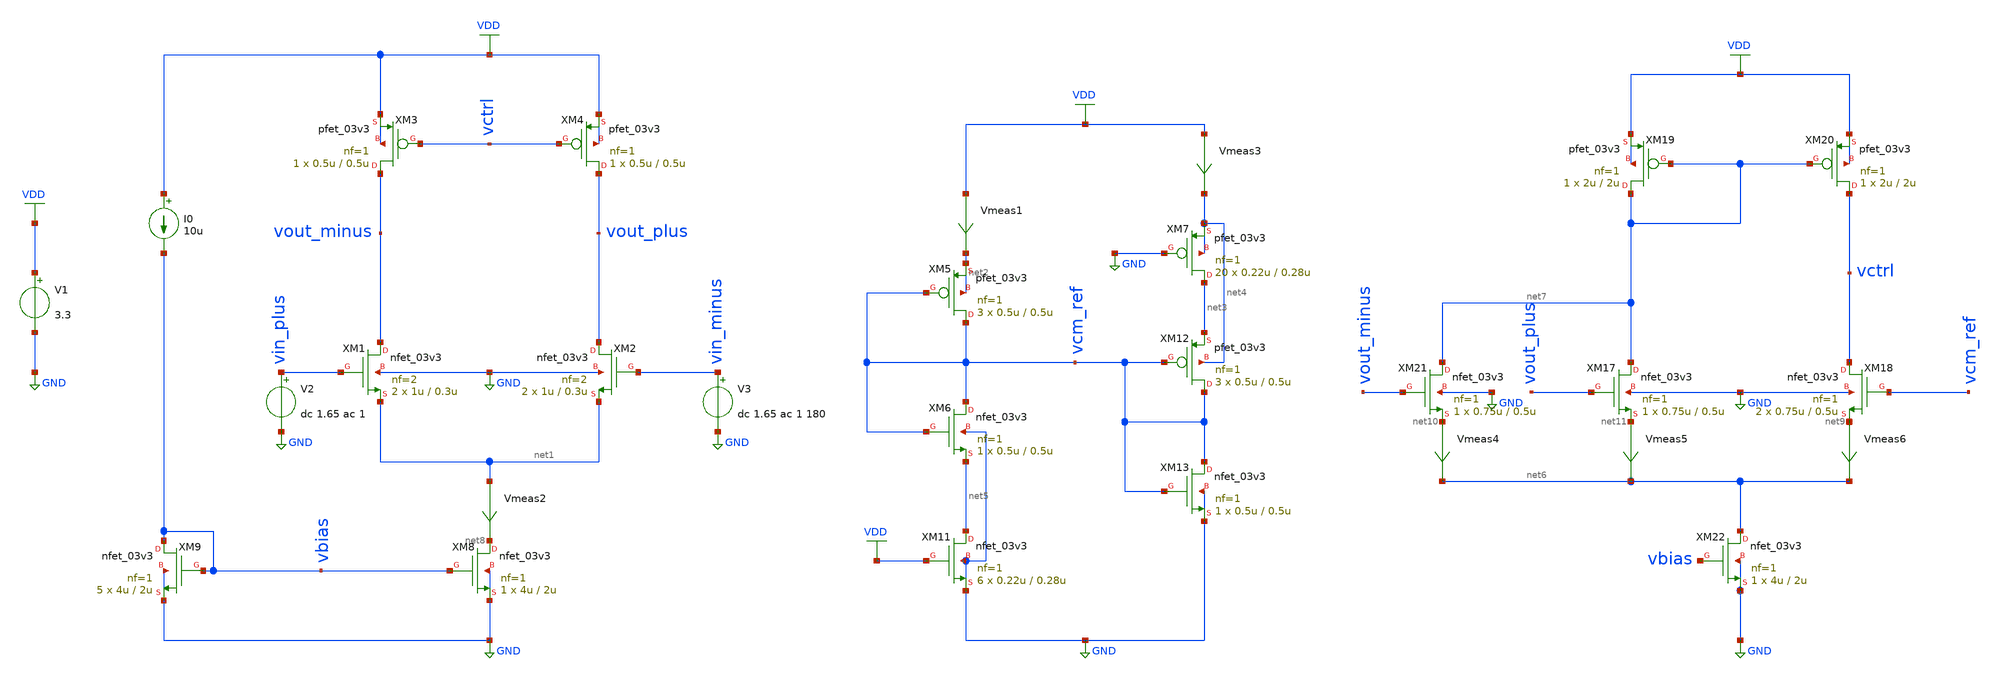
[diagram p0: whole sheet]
** sch_path: Design_Files/RAMP_test_try1.sch
**.subckt RAMP_test_try1
XM1 vout_minus vin_plus net1 GND nfet_03v3 L=0.3u W=1u nf=2 ad='int((nf+1)/2) * W/nf * 0.18u' as='int((nf+2)/2) * W/nf * 0.18u'
+ pd='2*int((nf+1)/2) * (W/nf + 0.18u)' ps='2*int((nf+2)/2) * (W/nf + 0.18u)' nrd='0.18u / W' nrs='0.18u / W'
+ sa=0 sb=0 sd=0 m=2
XM3 vout_minus vctrl VDD VDD pfet_03v3 L=0.5u W=0.5u nf=1 ad='int((nf+1)/2) * W/nf * 0.18u' as='int((nf+2)/2) * W/nf * 0.18u'
+ pd='2*int((nf+1)/2) * (W/nf + 0.18u)' ps='2*int((nf+2)/2) * (W/nf + 0.18u)' nrd='0.18u / W' nrs='0.18u / W'
+ sa=0 sb=0 sd=0 m=1
V2 vin_plus GND dc 1.65 ac 1
XM8 net8 vbias GND GND nfet_03v3 L=2u W=4u nf=1 ad='int((nf+1)/2) * W/nf * 0.18u' as='int((nf+2)/2) * W/nf * 0.18u'
+ pd='2*int((nf+1)/2) * (W/nf + 0.18u)' ps='2*int((nf+2)/2) * (W/nf + 0.18u)' nrd='0.18u / W' nrs='0.18u / W'
+ sa=0 sb=0 sd=0 m=1
Vmeas2 net1 net8 0
.save i(vmeas2)
V3 vin_minus GND dc 1.65 ac 1 180
XM9 vbias vbias GND GND nfet_03v3 L=2u W=4u nf=1 ad='int((nf+1)/2) * W/nf * 0.18u' as='int((nf+2)/2) * W/nf * 0.18u'
+ pd='2*int((nf+1)/2) * (W/nf + 0.18u)' ps='2*int((nf+2)/2) * (W/nf + 0.18u)' nrd='0.18u / W' nrs='0.18u / W'
+ sa=0 sb=0 sd=0 m=5
I0 VDD vbias 10u
XM2 vout_plus vin_minus net1 GND nfet_03v3 L=0.3u W=1u nf=2 ad='int((nf+1)/2) * W/nf * 0.18u' as='int((nf+2)/2) * W/nf * 0.18u'
+ pd='2*int((nf+1)/2) * (W/nf + 0.18u)' ps='2*int((nf+2)/2) * (W/nf + 0.18u)' nrd='0.18u / W' nrs='0.18u / W'
+ sa=0 sb=0 sd=0 m=2
XM4 vout_plus vctrl VDD VDD pfet_03v3 L=0.5u W=0.5u nf=1 ad='int((nf+1)/2) * W/nf * 0.18u' as='int((nf+2)/2) * W/nf * 0.18u'
+ pd='2*int((nf+1)/2) * (W/nf + 0.18u)' ps='2*int((nf+2)/2) * (W/nf + 0.18u)' nrd='0.18u / W' nrs='0.18u / W'
+ sa=0 sb=0 sd=0 m=1
V1 VDD GND 3.3
Vmeas1 VDD net2 0
.save i(vmeas1)
Vmeas3 VDD net4 0
.save i(vmeas3)
XM5 vcm_ref vcm_ref net2 net2 pfet_03v3 L=0.5u W=0.5u nf=1 ad='int((nf+1)/2) * W/nf * 0.18u' as='int((nf+2)/2) * W/nf * 0.18u'
+ pd='2*int((nf+1)/2) * (W/nf + 0.18u)' ps='2*int((nf+2)/2) * (W/nf + 0.18u)' nrd='0.18u / W' nrs='0.18u / W'
+ sa=0 sb=0 sd=0 m=3
XM6 vcm_ref vcm_ref net5 GND nfet_03v3 L=0.5u W=0.5u nf=1 ad='int((nf+1)/2) * W/nf * 0.18u' as='int((nf+2)/2) * W/nf * 0.18u'
+ pd='2*int((nf+1)/2) * (W/nf + 0.18u)' ps='2*int((nf+2)/2) * (W/nf + 0.18u)' nrd='0.18u / W' nrs='0.18u / W'
+ sa=0 sb=0 sd=0 m=1
XM11 net5 VDD GND GND nfet_03v3 L=0.28u W=0.22u nf=1 ad='int((nf+1)/2) * W/nf * 0.18u' as='int((nf+2)/2) * W/nf * 0.18u'
+ pd='2*int((nf+1)/2) * (W/nf + 0.18u)' ps='2*int((nf+2)/2) * (W/nf + 0.18u)' nrd='0.18u / W' nrs='0.18u / W'
+ sa=0 sb=0 sd=0 m=6
XM13 vcm_ref vcm_ref GND GND nfet_03v3 L=0.5u W=0.5u nf=1 ad='int((nf+1)/2) * W/nf * 0.18u' as='int((nf+2)/2) * W/nf * 0.18u'
+ pd='2*int((nf+1)/2) * (W/nf + 0.18u)' ps='2*int((nf+2)/2) * (W/nf + 0.18u)' nrd='0.18u / W' nrs='0.18u / W'
+ sa=0 sb=0 sd=0 m=1
XM12 vcm_ref vcm_ref net3 net4 pfet_03v3 L=0.5u W=0.5u nf=1 ad='int((nf+1)/2) * W/nf * 0.18u' as='int((nf+2)/2) * W/nf * 0.18u'
+ pd='2*int((nf+1)/2) * (W/nf + 0.18u)' ps='2*int((nf+2)/2) * (W/nf + 0.18u)' nrd='0.18u / W' nrs='0.18u / W'
+ sa=0 sb=0 sd=0 m=3
XM7 net3 GND net4 net4 pfet_03v3 L=0.28u W=0.22u nf=1 ad='int((nf+1)/2) * W/nf * 0.18u' as='int((nf+2)/2) * W/nf * 0.18u'
+ pd='2*int((nf+1)/2) * (W/nf + 0.18u)' ps='2*int((nf+2)/2) * (W/nf + 0.18u)' nrd='0.18u / W' nrs='0.18u / W'
+ sa=0 sb=0 sd=0 m=20
XM18 vctrl vcm_ref net9 GND nfet_03v3 L=0.5u W=0.75u nf=1 ad='int((nf+1)/2) * W/nf * 0.18u' as='int((nf+2)/2) * W/nf * 0.18u'
+ pd='2*int((nf+1)/2) * (W/nf + 0.18u)' ps='2*int((nf+2)/2) * (W/nf + 0.18u)' nrd='0.18u / W' nrs='0.18u / W'
+ sa=0 sb=0 sd=0 m=2
XM19 net7 net7 VDD VDD pfet_03v3 L=2u W=2u nf=1 ad='int((nf+1)/2) * W/nf * 0.18u' as='int((nf+2)/2) * W/nf * 0.18u'
+ pd='2*int((nf+1)/2) * (W/nf + 0.18u)' ps='2*int((nf+2)/2) * (W/nf + 0.18u)' nrd='0.18u / W' nrs='0.18u / W'
+ sa=0 sb=0 sd=0 m=1
XM20 vctrl net7 VDD VDD pfet_03v3 L=2u W=2u nf=1 ad='int((nf+1)/2) * W/nf * 0.18u' as='int((nf+2)/2) * W/nf * 0.18u'
+ pd='2*int((nf+1)/2) * (W/nf + 0.18u)' ps='2*int((nf+2)/2) * (W/nf + 0.18u)' nrd='0.18u / W' nrs='0.18u / W'
+ sa=0 sb=0 sd=0 m=1
XM21 net7 vout_minus net10 GND nfet_03v3 L=0.5u W=0.75u nf=1 ad='int((nf+1)/2) * W/nf * 0.18u' as='int((nf+2)/2) * W/nf * 0.18u'
+ pd='2*int((nf+1)/2) * (W/nf + 0.18u)' ps='2*int((nf+2)/2) * (W/nf + 0.18u)' nrd='0.18u / W' nrs='0.18u / W'
+ sa=0 sb=0 sd=0 m=1
XM22 net6 vbias GND GND nfet_03v3 L=2u W=4u nf=1 ad='int((nf+1)/2) * W/nf * 0.18u' as='int((nf+2)/2) * W/nf * 0.18u'
+ pd='2*int((nf+1)/2) * (W/nf + 0.18u)' ps='2*int((nf+2)/2) * (W/nf + 0.18u)' nrd='0.18u / W' nrs='0.18u / W'
+ sa=0 sb=0 sd=0 m=1
XM17 net7 vout_plus net11 GND nfet_03v3 L=0.5u W=0.75u nf=1 ad='int((nf+1)/2) * W/nf * 0.18u' as='int((nf+2)/2) * W/nf * 0.18u'
+ pd='2*int((nf+1)/2) * (W/nf + 0.18u)' ps='2*int((nf+2)/2) * (W/nf + 0.18u)' nrd='0.18u / W' nrs='0.18u / W'
+ sa=0 sb=0 sd=0 m=1
Vmeas4 net10 net6 0
.save i(vmeas4)
Vmeas5 net11 net6 0
.save i(vmeas5)
Vmeas6 net9 net6 0
.save i(vmeas6)
**.ends
.GLOBAL VDD
.GLOBAL GND
.end
